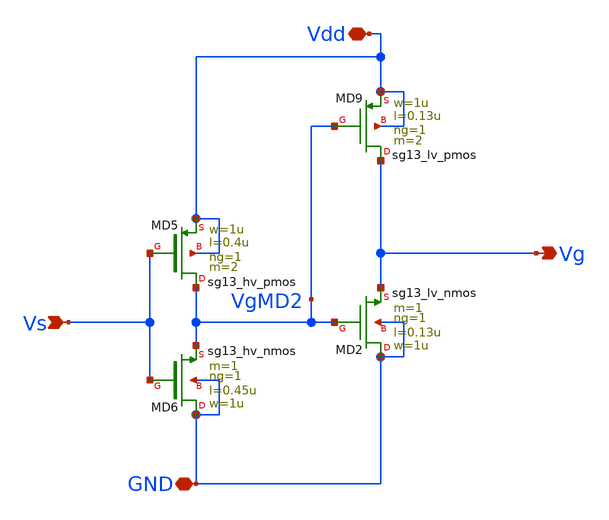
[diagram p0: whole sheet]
** sch_path: xschem/LevelShifter_HL_v2p1.sch
**.subckt LevelShifter_HL_v2p1 Vdd Vs Vg GND
*.iopin Vdd
*.ipin Vs
*.opin Vg
*.iopin GND
XMD9 Vg VgMD2 Vdd Vdd sg13_lv_pmos w=1u l=0.13u ng=1 m=2 mm_ok=1
XMD5 VgMD2 Vs Vdd Vdd sg13_hv_pmos w=1u l=0.4u ng=1 m=2 mm_ok=1
XMD6 GND Vs VgMD2 GND sg13_hv_nmos w=1u l=0.45u ng=1 m=1 mm_ok=1
XMD2 GND VgMD2 Vg GND sg13_lv_nmos w=1u l=0.13u ng=1 m=1 mm_ok=1
**.ends
.end
